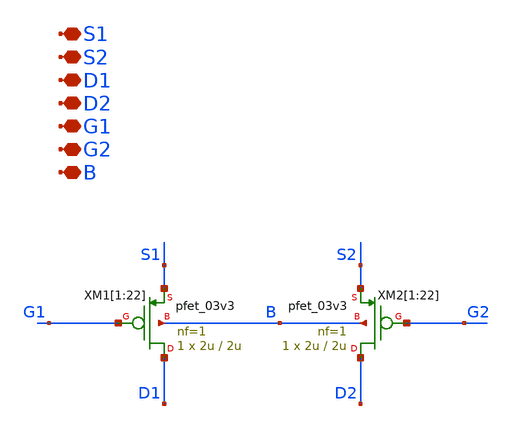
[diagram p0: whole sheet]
** sch_path: TIA_Filter/Folded/FC_pfets.sch
**.subckt FC_pfets S1 S2 D1 D2 G1 G2 B
*.iopin S1
*.iopin S2
*.iopin D1
*.iopin D2
*.iopin G1
*.iopin G2
*.iopin B
XM1[1] D1 G1 S1 B pfet_03v3 L=2u W=2u nf=1 ad='int((nf+1)/2) * W/nf * 0.18u' as='int((nf+2)/2) * W/nf * 0.18u'
+ pd='2*int((nf+1)/2) * (W/nf + 0.18u)' ps='2*int((nf+2)/2) * (W/nf + 0.18u)' nrd='0.18u / W' nrs='0.18u / W'
+ sa=0 sb=0 sd=0 m=1
XM1[2] D1 G1 S1 B pfet_03v3 L=2u W=2u nf=1 ad='int((nf+1)/2) * W/nf * 0.18u' as='int((nf+2)/2) * W/nf * 0.18u'
+ pd='2*int((nf+1)/2) * (W/nf + 0.18u)' ps='2*int((nf+2)/2) * (W/nf + 0.18u)' nrd='0.18u / W' nrs='0.18u / W'
+ sa=0 sb=0 sd=0 m=1
XM1[3] D1 G1 S1 B pfet_03v3 L=2u W=2u nf=1 ad='int((nf+1)/2) * W/nf * 0.18u' as='int((nf+2)/2) * W/nf * 0.18u'
+ pd='2*int((nf+1)/2) * (W/nf + 0.18u)' ps='2*int((nf+2)/2) * (W/nf + 0.18u)' nrd='0.18u / W' nrs='0.18u / W'
+ sa=0 sb=0 sd=0 m=1
XM1[4] D1 G1 S1 B pfet_03v3 L=2u W=2u nf=1 ad='int((nf+1)/2) * W/nf * 0.18u' as='int((nf+2)/2) * W/nf * 0.18u'
+ pd='2*int((nf+1)/2) * (W/nf + 0.18u)' ps='2*int((nf+2)/2) * (W/nf + 0.18u)' nrd='0.18u / W' nrs='0.18u / W'
+ sa=0 sb=0 sd=0 m=1
XM1[5] D1 G1 S1 B pfet_03v3 L=2u W=2u nf=1 ad='int((nf+1)/2) * W/nf * 0.18u' as='int((nf+2)/2) * W/nf * 0.18u'
+ pd='2*int((nf+1)/2) * (W/nf + 0.18u)' ps='2*int((nf+2)/2) * (W/nf + 0.18u)' nrd='0.18u / W' nrs='0.18u / W'
+ sa=0 sb=0 sd=0 m=1
XM1[6] D1 G1 S1 B pfet_03v3 L=2u W=2u nf=1 ad='int((nf+1)/2) * W/nf * 0.18u' as='int((nf+2)/2) * W/nf * 0.18u'
+ pd='2*int((nf+1)/2) * (W/nf + 0.18u)' ps='2*int((nf+2)/2) * (W/nf + 0.18u)' nrd='0.18u / W' nrs='0.18u / W'
+ sa=0 sb=0 sd=0 m=1
XM1[7] D1 G1 S1 B pfet_03v3 L=2u W=2u nf=1 ad='int((nf+1)/2) * W/nf * 0.18u' as='int((nf+2)/2) * W/nf * 0.18u'
+ pd='2*int((nf+1)/2) * (W/nf + 0.18u)' ps='2*int((nf+2)/2) * (W/nf + 0.18u)' nrd='0.18u / W' nrs='0.18u / W'
+ sa=0 sb=0 sd=0 m=1
XM1[8] D1 G1 S1 B pfet_03v3 L=2u W=2u nf=1 ad='int((nf+1)/2) * W/nf * 0.18u' as='int((nf+2)/2) * W/nf * 0.18u'
+ pd='2*int((nf+1)/2) * (W/nf + 0.18u)' ps='2*int((nf+2)/2) * (W/nf + 0.18u)' nrd='0.18u / W' nrs='0.18u / W'
+ sa=0 sb=0 sd=0 m=1
XM1[9] D1 G1 S1 B pfet_03v3 L=2u W=2u nf=1 ad='int((nf+1)/2) * W/nf * 0.18u' as='int((nf+2)/2) * W/nf * 0.18u'
+ pd='2*int((nf+1)/2) * (W/nf + 0.18u)' ps='2*int((nf+2)/2) * (W/nf + 0.18u)' nrd='0.18u / W' nrs='0.18u / W'
+ sa=0 sb=0 sd=0 m=1
XM1[10] D1 G1 S1 B pfet_03v3 L=2u W=2u nf=1 ad='int((nf+1)/2) * W/nf * 0.18u' as='int((nf+2)/2) * W/nf * 0.18u'
+ pd='2*int((nf+1)/2) * (W/nf + 0.18u)' ps='2*int((nf+2)/2) * (W/nf + 0.18u)' nrd='0.18u / W' nrs='0.18u / W'
+ sa=0 sb=0 sd=0 m=1
XM1[11] D1 G1 S1 B pfet_03v3 L=2u W=2u nf=1 ad='int((nf+1)/2) * W/nf * 0.18u' as='int((nf+2)/2) * W/nf * 0.18u'
+ pd='2*int((nf+1)/2) * (W/nf + 0.18u)' ps='2*int((nf+2)/2) * (W/nf + 0.18u)' nrd='0.18u / W' nrs='0.18u / W'
+ sa=0 sb=0 sd=0 m=1
XM1[12] D1 G1 S1 B pfet_03v3 L=2u W=2u nf=1 ad='int((nf+1)/2) * W/nf * 0.18u' as='int((nf+2)/2) * W/nf * 0.18u'
+ pd='2*int((nf+1)/2) * (W/nf + 0.18u)' ps='2*int((nf+2)/2) * (W/nf + 0.18u)' nrd='0.18u / W' nrs='0.18u / W'
+ sa=0 sb=0 sd=0 m=1
XM1[13] D1 G1 S1 B pfet_03v3 L=2u W=2u nf=1 ad='int((nf+1)/2) * W/nf * 0.18u' as='int((nf+2)/2) * W/nf * 0.18u'
+ pd='2*int((nf+1)/2) * (W/nf + 0.18u)' ps='2*int((nf+2)/2) * (W/nf + 0.18u)' nrd='0.18u / W' nrs='0.18u / W'
+ sa=0 sb=0 sd=0 m=1
XM1[14] D1 G1 S1 B pfet_03v3 L=2u W=2u nf=1 ad='int((nf+1)/2) * W/nf * 0.18u' as='int((nf+2)/2) * W/nf * 0.18u'
+ pd='2*int((nf+1)/2) * (W/nf + 0.18u)' ps='2*int((nf+2)/2) * (W/nf + 0.18u)' nrd='0.18u / W' nrs='0.18u / W'
+ sa=0 sb=0 sd=0 m=1
XM1[15] D1 G1 S1 B pfet_03v3 L=2u W=2u nf=1 ad='int((nf+1)/2) * W/nf * 0.18u' as='int((nf+2)/2) * W/nf * 0.18u'
+ pd='2*int((nf+1)/2) * (W/nf + 0.18u)' ps='2*int((nf+2)/2) * (W/nf + 0.18u)' nrd='0.18u / W' nrs='0.18u / W'
+ sa=0 sb=0 sd=0 m=1
XM1[16] D1 G1 S1 B pfet_03v3 L=2u W=2u nf=1 ad='int((nf+1)/2) * W/nf * 0.18u' as='int((nf+2)/2) * W/nf * 0.18u'
+ pd='2*int((nf+1)/2) * (W/nf + 0.18u)' ps='2*int((nf+2)/2) * (W/nf + 0.18u)' nrd='0.18u / W' nrs='0.18u / W'
+ sa=0 sb=0 sd=0 m=1
XM1[17] D1 G1 S1 B pfet_03v3 L=2u W=2u nf=1 ad='int((nf+1)/2) * W/nf * 0.18u' as='int((nf+2)/2) * W/nf * 0.18u'
+ pd='2*int((nf+1)/2) * (W/nf + 0.18u)' ps='2*int((nf+2)/2) * (W/nf + 0.18u)' nrd='0.18u / W' nrs='0.18u / W'
+ sa=0 sb=0 sd=0 m=1
XM1[18] D1 G1 S1 B pfet_03v3 L=2u W=2u nf=1 ad='int((nf+1)/2) * W/nf * 0.18u' as='int((nf+2)/2) * W/nf * 0.18u'
+ pd='2*int((nf+1)/2) * (W/nf + 0.18u)' ps='2*int((nf+2)/2) * (W/nf + 0.18u)' nrd='0.18u / W' nrs='0.18u / W'
+ sa=0 sb=0 sd=0 m=1
XM1[19] D1 G1 S1 B pfet_03v3 L=2u W=2u nf=1 ad='int((nf+1)/2) * W/nf * 0.18u' as='int((nf+2)/2) * W/nf * 0.18u'
+ pd='2*int((nf+1)/2) * (W/nf + 0.18u)' ps='2*int((nf+2)/2) * (W/nf + 0.18u)' nrd='0.18u / W' nrs='0.18u / W'
+ sa=0 sb=0 sd=0 m=1
XM1[20] D1 G1 S1 B pfet_03v3 L=2u W=2u nf=1 ad='int((nf+1)/2) * W/nf * 0.18u' as='int((nf+2)/2) * W/nf * 0.18u'
+ pd='2*int((nf+1)/2) * (W/nf + 0.18u)' ps='2*int((nf+2)/2) * (W/nf + 0.18u)' nrd='0.18u / W' nrs='0.18u / W'
+ sa=0 sb=0 sd=0 m=1
XM1[21] D1 G1 S1 B pfet_03v3 L=2u W=2u nf=1 ad='int((nf+1)/2) * W/nf * 0.18u' as='int((nf+2)/2) * W/nf * 0.18u'
+ pd='2*int((nf+1)/2) * (W/nf + 0.18u)' ps='2*int((nf+2)/2) * (W/nf + 0.18u)' nrd='0.18u / W' nrs='0.18u / W'
+ sa=0 sb=0 sd=0 m=1
XM1[22] D1 G1 S1 B pfet_03v3 L=2u W=2u nf=1 ad='int((nf+1)/2) * W/nf * 0.18u' as='int((nf+2)/2) * W/nf * 0.18u'
+ pd='2*int((nf+1)/2) * (W/nf + 0.18u)' ps='2*int((nf+2)/2) * (W/nf + 0.18u)' nrd='0.18u / W' nrs='0.18u / W'
+ sa=0 sb=0 sd=0 m=1
XM2[1] D2 G2 S2 B pfet_03v3 L=2u W=2u nf=1 ad='int((nf+1)/2) * W/nf * 0.18u' as='int((nf+2)/2) * W/nf * 0.18u'
+ pd='2*int((nf+1)/2) * (W/nf + 0.18u)' ps='2*int((nf+2)/2) * (W/nf + 0.18u)' nrd='0.18u / W' nrs='0.18u / W'
+ sa=0 sb=0 sd=0 m=1
XM2[2] D2 G2 S2 B pfet_03v3 L=2u W=2u nf=1 ad='int((nf+1)/2) * W/nf * 0.18u' as='int((nf+2)/2) * W/nf * 0.18u'
+ pd='2*int((nf+1)/2) * (W/nf + 0.18u)' ps='2*int((nf+2)/2) * (W/nf + 0.18u)' nrd='0.18u / W' nrs='0.18u / W'
+ sa=0 sb=0 sd=0 m=1
XM2[3] D2 G2 S2 B pfet_03v3 L=2u W=2u nf=1 ad='int((nf+1)/2) * W/nf * 0.18u' as='int((nf+2)/2) * W/nf * 0.18u'
+ pd='2*int((nf+1)/2) * (W/nf + 0.18u)' ps='2*int((nf+2)/2) * (W/nf + 0.18u)' nrd='0.18u / W' nrs='0.18u / W'
+ sa=0 sb=0 sd=0 m=1
XM2[4] D2 G2 S2 B pfet_03v3 L=2u W=2u nf=1 ad='int((nf+1)/2) * W/nf * 0.18u' as='int((nf+2)/2) * W/nf * 0.18u'
+ pd='2*int((nf+1)/2) * (W/nf + 0.18u)' ps='2*int((nf+2)/2) * (W/nf + 0.18u)' nrd='0.18u / W' nrs='0.18u / W'
+ sa=0 sb=0 sd=0 m=1
XM2[5] D2 G2 S2 B pfet_03v3 L=2u W=2u nf=1 ad='int((nf+1)/2) * W/nf * 0.18u' as='int((nf+2)/2) * W/nf * 0.18u'
+ pd='2*int((nf+1)/2) * (W/nf + 0.18u)' ps='2*int((nf+2)/2) * (W/nf + 0.18u)' nrd='0.18u / W' nrs='0.18u / W'
+ sa=0 sb=0 sd=0 m=1
XM2[6] D2 G2 S2 B pfet_03v3 L=2u W=2u nf=1 ad='int((nf+1)/2) * W/nf * 0.18u' as='int((nf+2)/2) * W/nf * 0.18u'
+ pd='2*int((nf+1)/2) * (W/nf + 0.18u)' ps='2*int((nf+2)/2) * (W/nf + 0.18u)' nrd='0.18u / W' nrs='0.18u / W'
+ sa=0 sb=0 sd=0 m=1
XM2[7] D2 G2 S2 B pfet_03v3 L=2u W=2u nf=1 ad='int((nf+1)/2) * W/nf * 0.18u' as='int((nf+2)/2) * W/nf * 0.18u'
+ pd='2*int((nf+1)/2) * (W/nf + 0.18u)' ps='2*int((nf+2)/2) * (W/nf + 0.18u)' nrd='0.18u / W' nrs='0.18u / W'
+ sa=0 sb=0 sd=0 m=1
XM2[8] D2 G2 S2 B pfet_03v3 L=2u W=2u nf=1 ad='int((nf+1)/2) * W/nf * 0.18u' as='int((nf+2)/2) * W/nf * 0.18u'
+ pd='2*int((nf+1)/2) * (W/nf + 0.18u)' ps='2*int((nf+2)/2) * (W/nf + 0.18u)' nrd='0.18u / W' nrs='0.18u / W'
+ sa=0 sb=0 sd=0 m=1
XM2[9] D2 G2 S2 B pfet_03v3 L=2u W=2u nf=1 ad='int((nf+1)/2) * W/nf * 0.18u' as='int((nf+2)/2) * W/nf * 0.18u'
+ pd='2*int((nf+1)/2) * (W/nf + 0.18u)' ps='2*int((nf+2)/2) * (W/nf + 0.18u)' nrd='0.18u / W' nrs='0.18u / W'
+ sa=0 sb=0 sd=0 m=1
XM2[10] D2 G2 S2 B pfet_03v3 L=2u W=2u nf=1 ad='int((nf+1)/2) * W/nf * 0.18u' as='int((nf+2)/2) * W/nf * 0.18u'
+ pd='2*int((nf+1)/2) * (W/nf + 0.18u)' ps='2*int((nf+2)/2) * (W/nf + 0.18u)' nrd='0.18u / W' nrs='0.18u / W'
+ sa=0 sb=0 sd=0 m=1
XM2[11] D2 G2 S2 B pfet_03v3 L=2u W=2u nf=1 ad='int((nf+1)/2) * W/nf * 0.18u' as='int((nf+2)/2) * W/nf * 0.18u'
+ pd='2*int((nf+1)/2) * (W/nf + 0.18u)' ps='2*int((nf+2)/2) * (W/nf + 0.18u)' nrd='0.18u / W' nrs='0.18u / W'
+ sa=0 sb=0 sd=0 m=1
XM2[12] D2 G2 S2 B pfet_03v3 L=2u W=2u nf=1 ad='int((nf+1)/2) * W/nf * 0.18u' as='int((nf+2)/2) * W/nf * 0.18u'
+ pd='2*int((nf+1)/2) * (W/nf + 0.18u)' ps='2*int((nf+2)/2) * (W/nf + 0.18u)' nrd='0.18u / W' nrs='0.18u / W'
+ sa=0 sb=0 sd=0 m=1
XM2[13] D2 G2 S2 B pfet_03v3 L=2u W=2u nf=1 ad='int((nf+1)/2) * W/nf * 0.18u' as='int((nf+2)/2) * W/nf * 0.18u'
+ pd='2*int((nf+1)/2) * (W/nf + 0.18u)' ps='2*int((nf+2)/2) * (W/nf + 0.18u)' nrd='0.18u / W' nrs='0.18u / W'
+ sa=0 sb=0 sd=0 m=1
XM2[14] D2 G2 S2 B pfet_03v3 L=2u W=2u nf=1 ad='int((nf+1)/2) * W/nf * 0.18u' as='int((nf+2)/2) * W/nf * 0.18u'
+ pd='2*int((nf+1)/2) * (W/nf + 0.18u)' ps='2*int((nf+2)/2) * (W/nf + 0.18u)' nrd='0.18u / W' nrs='0.18u / W'
+ sa=0 sb=0 sd=0 m=1
XM2[15] D2 G2 S2 B pfet_03v3 L=2u W=2u nf=1 ad='int((nf+1)/2) * W/nf * 0.18u' as='int((nf+2)/2) * W/nf * 0.18u'
+ pd='2*int((nf+1)/2) * (W/nf + 0.18u)' ps='2*int((nf+2)/2) * (W/nf + 0.18u)' nrd='0.18u / W' nrs='0.18u / W'
+ sa=0 sb=0 sd=0 m=1
XM2[16] D2 G2 S2 B pfet_03v3 L=2u W=2u nf=1 ad='int((nf+1)/2) * W/nf * 0.18u' as='int((nf+2)/2) * W/nf * 0.18u'
+ pd='2*int((nf+1)/2) * (W/nf + 0.18u)' ps='2*int((nf+2)/2) * (W/nf + 0.18u)' nrd='0.18u / W' nrs='0.18u / W'
+ sa=0 sb=0 sd=0 m=1
XM2[17] D2 G2 S2 B pfet_03v3 L=2u W=2u nf=1 ad='int((nf+1)/2) * W/nf * 0.18u' as='int((nf+2)/2) * W/nf * 0.18u'
+ pd='2*int((nf+1)/2) * (W/nf + 0.18u)' ps='2*int((nf+2)/2) * (W/nf + 0.18u)' nrd='0.18u / W' nrs='0.18u / W'
+ sa=0 sb=0 sd=0 m=1
XM2[18] D2 G2 S2 B pfet_03v3 L=2u W=2u nf=1 ad='int((nf+1)/2) * W/nf * 0.18u' as='int((nf+2)/2) * W/nf * 0.18u'
+ pd='2*int((nf+1)/2) * (W/nf + 0.18u)' ps='2*int((nf+2)/2) * (W/nf + 0.18u)' nrd='0.18u / W' nrs='0.18u / W'
+ sa=0 sb=0 sd=0 m=1
XM2[19] D2 G2 S2 B pfet_03v3 L=2u W=2u nf=1 ad='int((nf+1)/2) * W/nf * 0.18u' as='int((nf+2)/2) * W/nf * 0.18u'
+ pd='2*int((nf+1)/2) * (W/nf + 0.18u)' ps='2*int((nf+2)/2) * (W/nf + 0.18u)' nrd='0.18u / W' nrs='0.18u / W'
+ sa=0 sb=0 sd=0 m=1
XM2[20] D2 G2 S2 B pfet_03v3 L=2u W=2u nf=1 ad='int((nf+1)/2) * W/nf * 0.18u' as='int((nf+2)/2) * W/nf * 0.18u'
+ pd='2*int((nf+1)/2) * (W/nf + 0.18u)' ps='2*int((nf+2)/2) * (W/nf + 0.18u)' nrd='0.18u / W' nrs='0.18u / W'
+ sa=0 sb=0 sd=0 m=1
XM2[21] D2 G2 S2 B pfet_03v3 L=2u W=2u nf=1 ad='int((nf+1)/2) * W/nf * 0.18u' as='int((nf+2)/2) * W/nf * 0.18u'
+ pd='2*int((nf+1)/2) * (W/nf + 0.18u)' ps='2*int((nf+2)/2) * (W/nf + 0.18u)' nrd='0.18u / W' nrs='0.18u / W'
+ sa=0 sb=0 sd=0 m=1
XM2[22] D2 G2 S2 B pfet_03v3 L=2u W=2u nf=1 ad='int((nf+1)/2) * W/nf * 0.18u' as='int((nf+2)/2) * W/nf * 0.18u'
+ pd='2*int((nf+1)/2) * (W/nf + 0.18u)' ps='2*int((nf+2)/2) * (W/nf + 0.18u)' nrd='0.18u / W' nrs='0.18u / W'
+ sa=0 sb=0 sd=0 m=1
**.ends
.end
